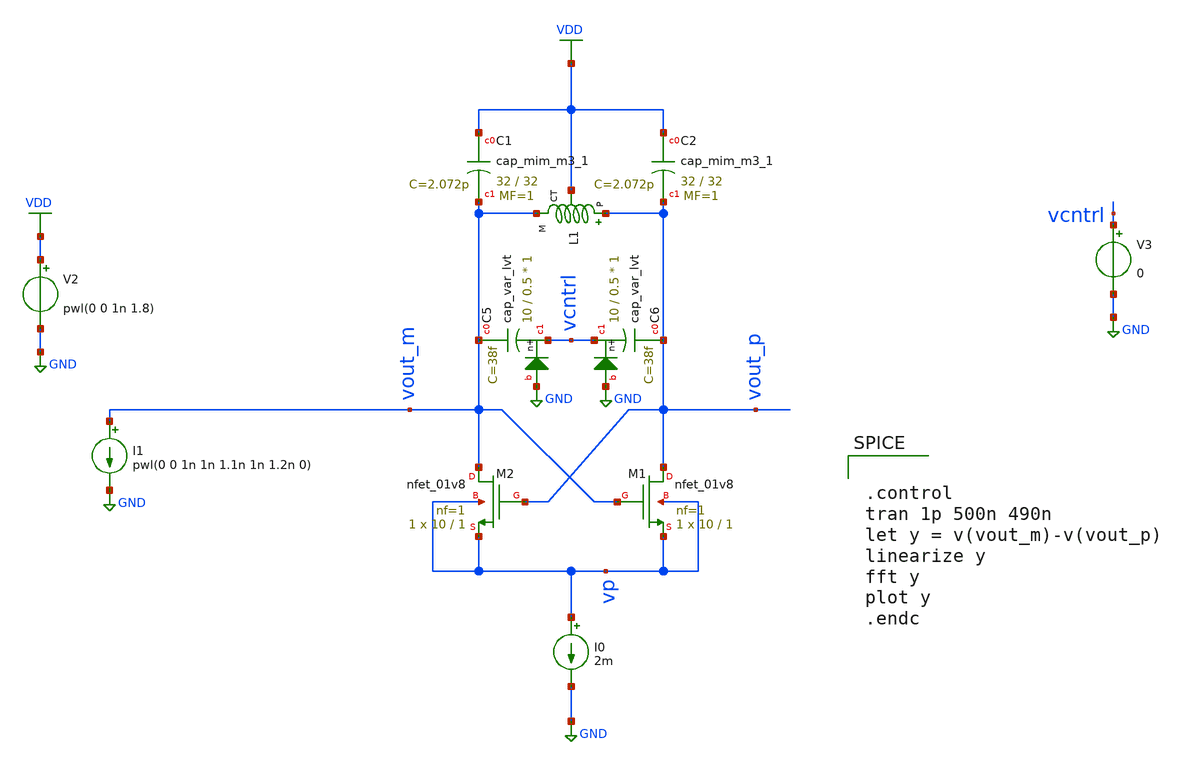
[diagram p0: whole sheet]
** sch_path: vco_pdkmosftet.sch
**.subckt vco_pdkmosftet
I0 vp GND 2m
V2 VDD GND pwl(0 0 1n 1.8)
V3 vcntrl GND 0
XC5 vout_m vcntrl GND sky130_fd_pr__cap_var_lvt W=10 L=0.5 VM=1 m=1
XC6 vout_p vcntrl GND sky130_fd_pr__cap_var_lvt W=10 L=0.5 VM=1 m=1
I1 vout_m GND pwl(0 0 1n 1n 1.1n 1n 1.2n 0)
XM1 vout_p vout_m vp vp sky130_fd_pr__nfet_01v8 L=1 W=10 nf=1 ad='int((nf+1)/2) * W/nf * 0.29' as='int((nf+2)/2) * W/nf * 0.29'
+ pd='2*int((nf+1)/2) * (W/nf + 0.29)' ps='2*int((nf+2)/2) * (W/nf + 0.29)' nrd='0.29 / W' nrs='0.29 / W'
+ sa=0 sb=0 sd=0 mult=1 m=1
XM2 vout_m vout_p vp vp sky130_fd_pr__nfet_01v8 L=1 W=10 nf=1 ad='int((nf+1)/2) * W/nf * 0.29' as='int((nf+2)/2) * W/nf * 0.29'
+ pd='2*int((nf+1)/2) * (W/nf + 0.29)' ps='2*int((nf+2)/2) * (W/nf + 0.29)' nrd='0.29 / W' nrs='0.29 / W'
+ sa=0 sb=0 sd=0 mult=1 m=1
XC1 VDD vout_m sky130_fd_pr__cap_mim_m3_1 W=32 L=32 MF=1 m=1
XC2 VDD vout_p sky130_fd_pr__cap_mim_m3_1 W=32 L=32 MF=1 m=1
XL1 vout_p vout_m VDD GND sky130_fd_pr__ind_05_220
**** begin user architecture code


.option wnflag = 1
.lib /usr/local/share/pdk/sky130A/libs.tech/ngspice/sky130.lib.spice tt
.include /usr/local/share/pdk/sky130A/libs.ref/sky130_fd_pr/spice/sky130_fd_pr__ind_05_220.model.spice
.param mc_mm_switch=0




.control
tran 1p 500n 490n
let y = v(vout_m)-v(vout_p)
linearize y
fft y
plot y
.endc


**** end user architecture code
**.ends
.GLOBAL VDD
.GLOBAL GND
.end
